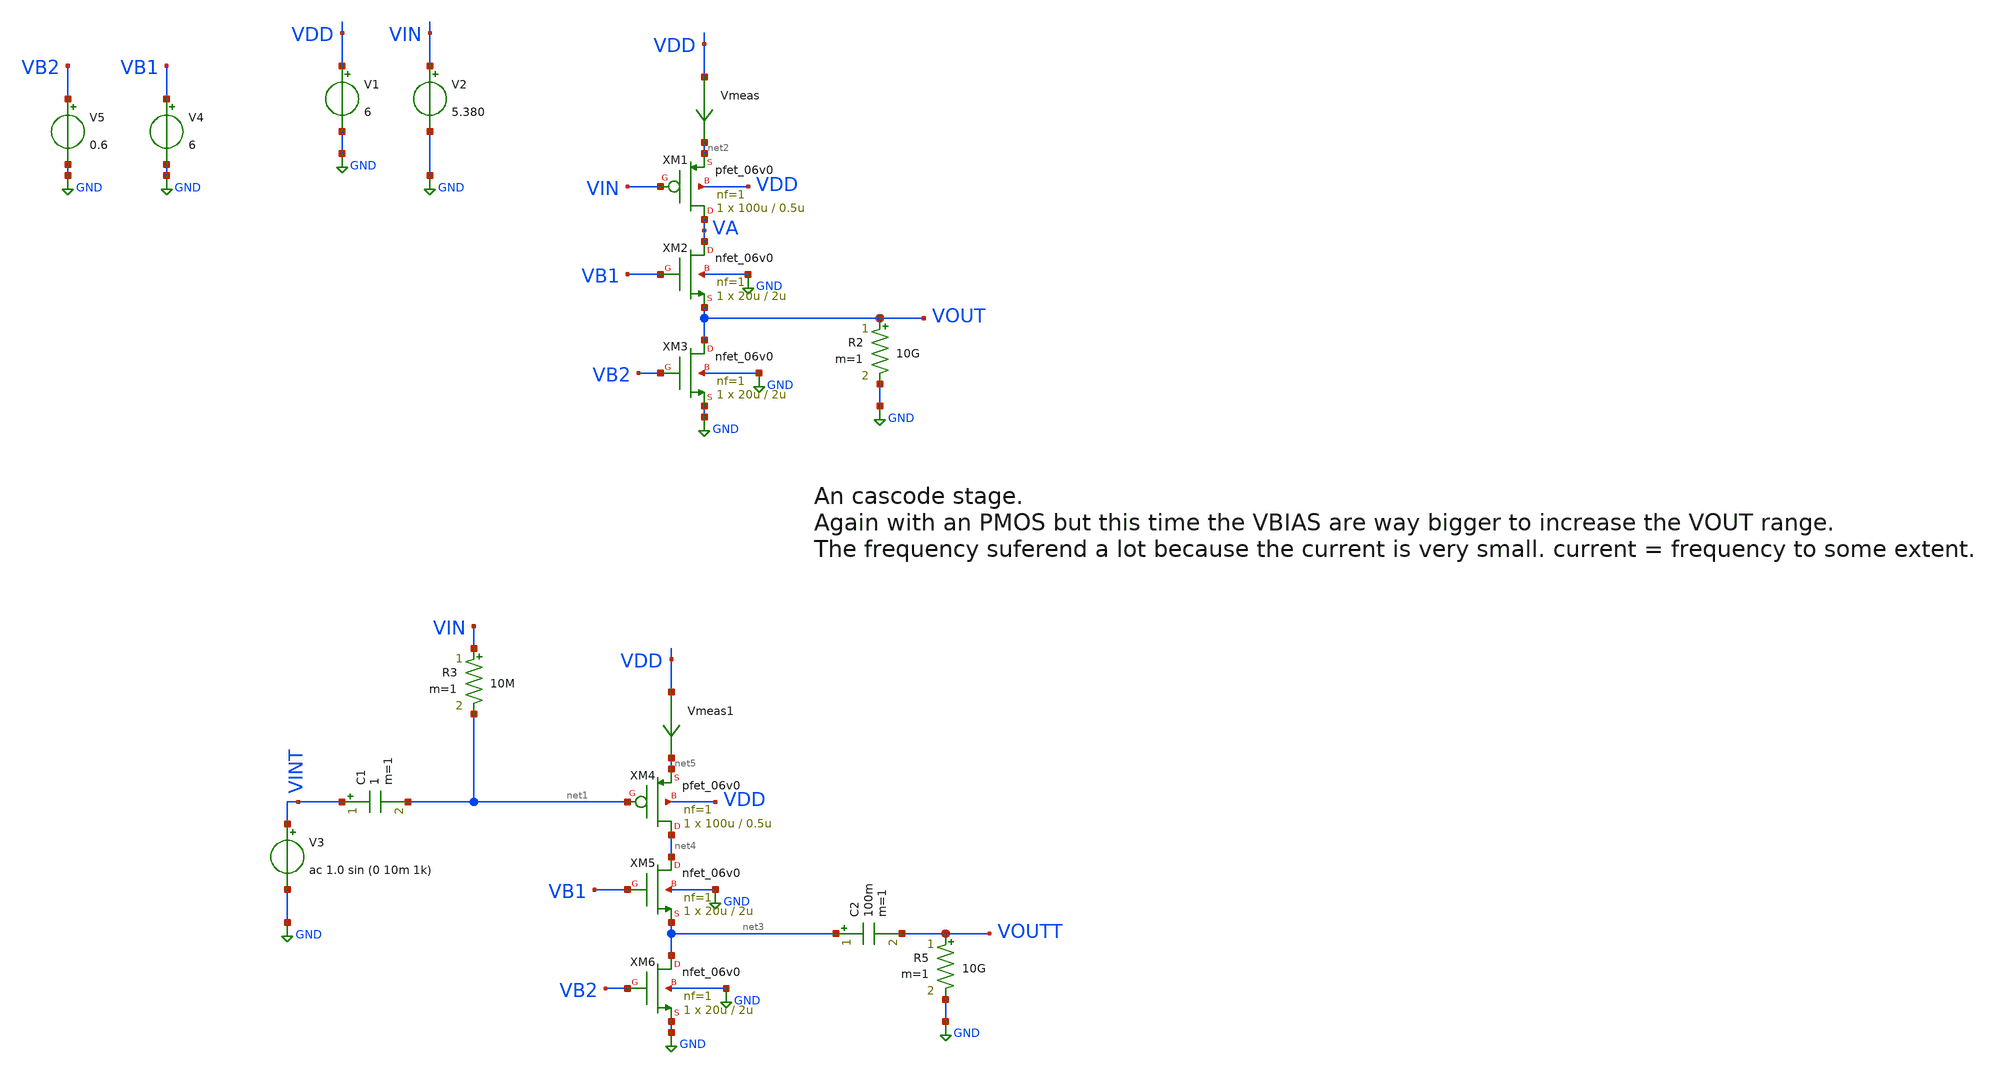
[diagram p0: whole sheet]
** sch_path: unusual_amplifiers/unusual_amp12.sch
**.subckt unusual_amp12
Vmeas VDD net2 0
.save i(vmeas)
V1 VDD GND 6
V2 VIN GND 5.380
V3 VINT GND ac 1.0 sin (0 10m 1k)
R2 VOUT GND 10G m=1
C1 VINT net1 1 m=1
R3 VIN net1 10M m=1
C2 net3 VOUTT 100m m=1
R5 VOUTT GND 10G m=1
V4 VB1 GND 6
XM1 VA VIN net2 VDD pfet_06v0 L=0.5u W=100u nf=1 ad='int((nf+1)/2) * W/nf * 0.18u' as='int((nf+2)/2) * W/nf * 0.18u'
+ pd='2*int((nf+1)/2) * (W/nf + 0.18u)' ps='2*int((nf+2)/2) * (W/nf + 0.18u)' nrd='0.18u / W' nrs='0.18u / W'
+ sa=0 sb=0 sd=0 m=1
XM2 VA VB1 VOUT GND nfet_06v0 L=2u W=20u nf=1 ad='int((nf+1)/2) * W/nf * 0.18u' as='int((nf+2)/2) * W/nf * 0.18u'
+ pd='2*int((nf+1)/2) * (W/nf + 0.18u)' ps='2*int((nf+2)/2) * (W/nf + 0.18u)' nrd='0.18u / W' nrs='0.18u / W'
+ sa=0 sb=0 sd=0 m=1
XM3 VOUT VB2 GND GND nfet_06v0 L=2u W=20u nf=1 ad='int((nf+1)/2) * W/nf * 0.18u' as='int((nf+2)/2) * W/nf * 0.18u'
+ pd='2*int((nf+1)/2) * (W/nf + 0.18u)' ps='2*int((nf+2)/2) * (W/nf + 0.18u)' nrd='0.18u / W' nrs='0.18u / W'
+ sa=0 sb=0 sd=0 m=1
V5 VB2 GND 0.6
Vmeas1 VDD net5 0
.save i(vmeas1)
XM4 net4 net1 net5 VDD pfet_06v0 L=0.5u W=100u nf=1 ad='int((nf+1)/2) * W/nf * 0.18u' as='int((nf+2)/2) * W/nf * 0.18u'
+ pd='2*int((nf+1)/2) * (W/nf + 0.18u)' ps='2*int((nf+2)/2) * (W/nf + 0.18u)' nrd='0.18u / W' nrs='0.18u / W'
+ sa=0 sb=0 sd=0 m=1
XM5 net4 VB1 net3 GND nfet_06v0 L=2u W=20u nf=1 ad='int((nf+1)/2) * W/nf * 0.18u' as='int((nf+2)/2) * W/nf * 0.18u'
+ pd='2*int((nf+1)/2) * (W/nf + 0.18u)' ps='2*int((nf+2)/2) * (W/nf + 0.18u)' nrd='0.18u / W' nrs='0.18u / W'
+ sa=0 sb=0 sd=0 m=1
XM6 net3 VB2 GND GND nfet_06v0 L=2u W=20u nf=1 ad='int((nf+1)/2) * W/nf * 0.18u' as='int((nf+2)/2) * W/nf * 0.18u'
+ pd='2*int((nf+1)/2) * (W/nf + 0.18u)' ps='2*int((nf+2)/2) * (W/nf + 0.18u)' nrd='0.18u / W' nrs='0.18u / W'
+ sa=0 sb=0 sd=0 m=1
**** begin user architecture code

**************************************************************
**************************************************************
**************************************************************
**************************************************************
**************************************************************
*LIBs*********************************************************
**************************************************************
**************************************************************
**************************************************************
**************************************************************
**************************************************************
.include $::180MCU_MODELS/design.ngspice
*.lib $::180MCU_MODELS/sm141064.ngspice statistical *use statistical if you want global and parameter mismatch
*.lib $::180MCU_MODELS/sm141064.ngspice res_statistical
.lib $::180MCU_MODELS/sm141064.ngspice typical
.lib $::180MCU_MODELS/sm141064.ngspice res_typical
.lib $::180MCU_MODELS/sm141064.ngspice moscap_typical
.lib $::180MCU_MODELS/sm141064.ngspice bjt_typical
.lib $::180MCU_MODELS/sm141064.ngspice diode_typical
.lib $::180MCU_MODELS/sm141064.ngspice mimcap_typical
**************************************************************
**************************************************************
**************************************************************
**************************************************************
**************************************************************
*Corners/montecarlo options***********************************
**************************************************************
**************************************************************
**************************************************************
**************************************************************
**************************************************************
.TEMP 27
.param   sw_stat_global = 1   sw_stat_mism = 1  mc_skew = 3  res_mc_skew = 3  cap_mc_skew = 3
+  fnoicor = 1
**************************************************************
**************************************************************
**************************************************************
**************************************************************
*SIMULATION and Plots*****************************************
**************************************************************
**************************************************************
**************************************************************
**************************************************************
.control
save all
dc V2 0 6 0.01
*dc simulation
plot v(VOUT) v(VIN) deriv(v(VOUT)) v(VA)
plot v(VA)
*ploting VIN VOUT and the voltage gain
plot i(Vmeas)
*ploting the current for curiosity
tran 1us 2m
*transient simulation
plot (v(VINT)) (v(VOUTT))
*simple plot to exemplify the gain
fft v(VOUTT) v(VINT)
*fast fourier transfor
plot mag(v(VOUTT)) mag(v(VINT))
* analyse the frequency spectrum of the transient waves, to detect distortion
ac dec 20 1 50G
*simple ac simulation
plot v(VOUTT)
*gain in function of the input frequency
.endc

**** end user architecture code
**.ends
.GLOBAL GND
.end
